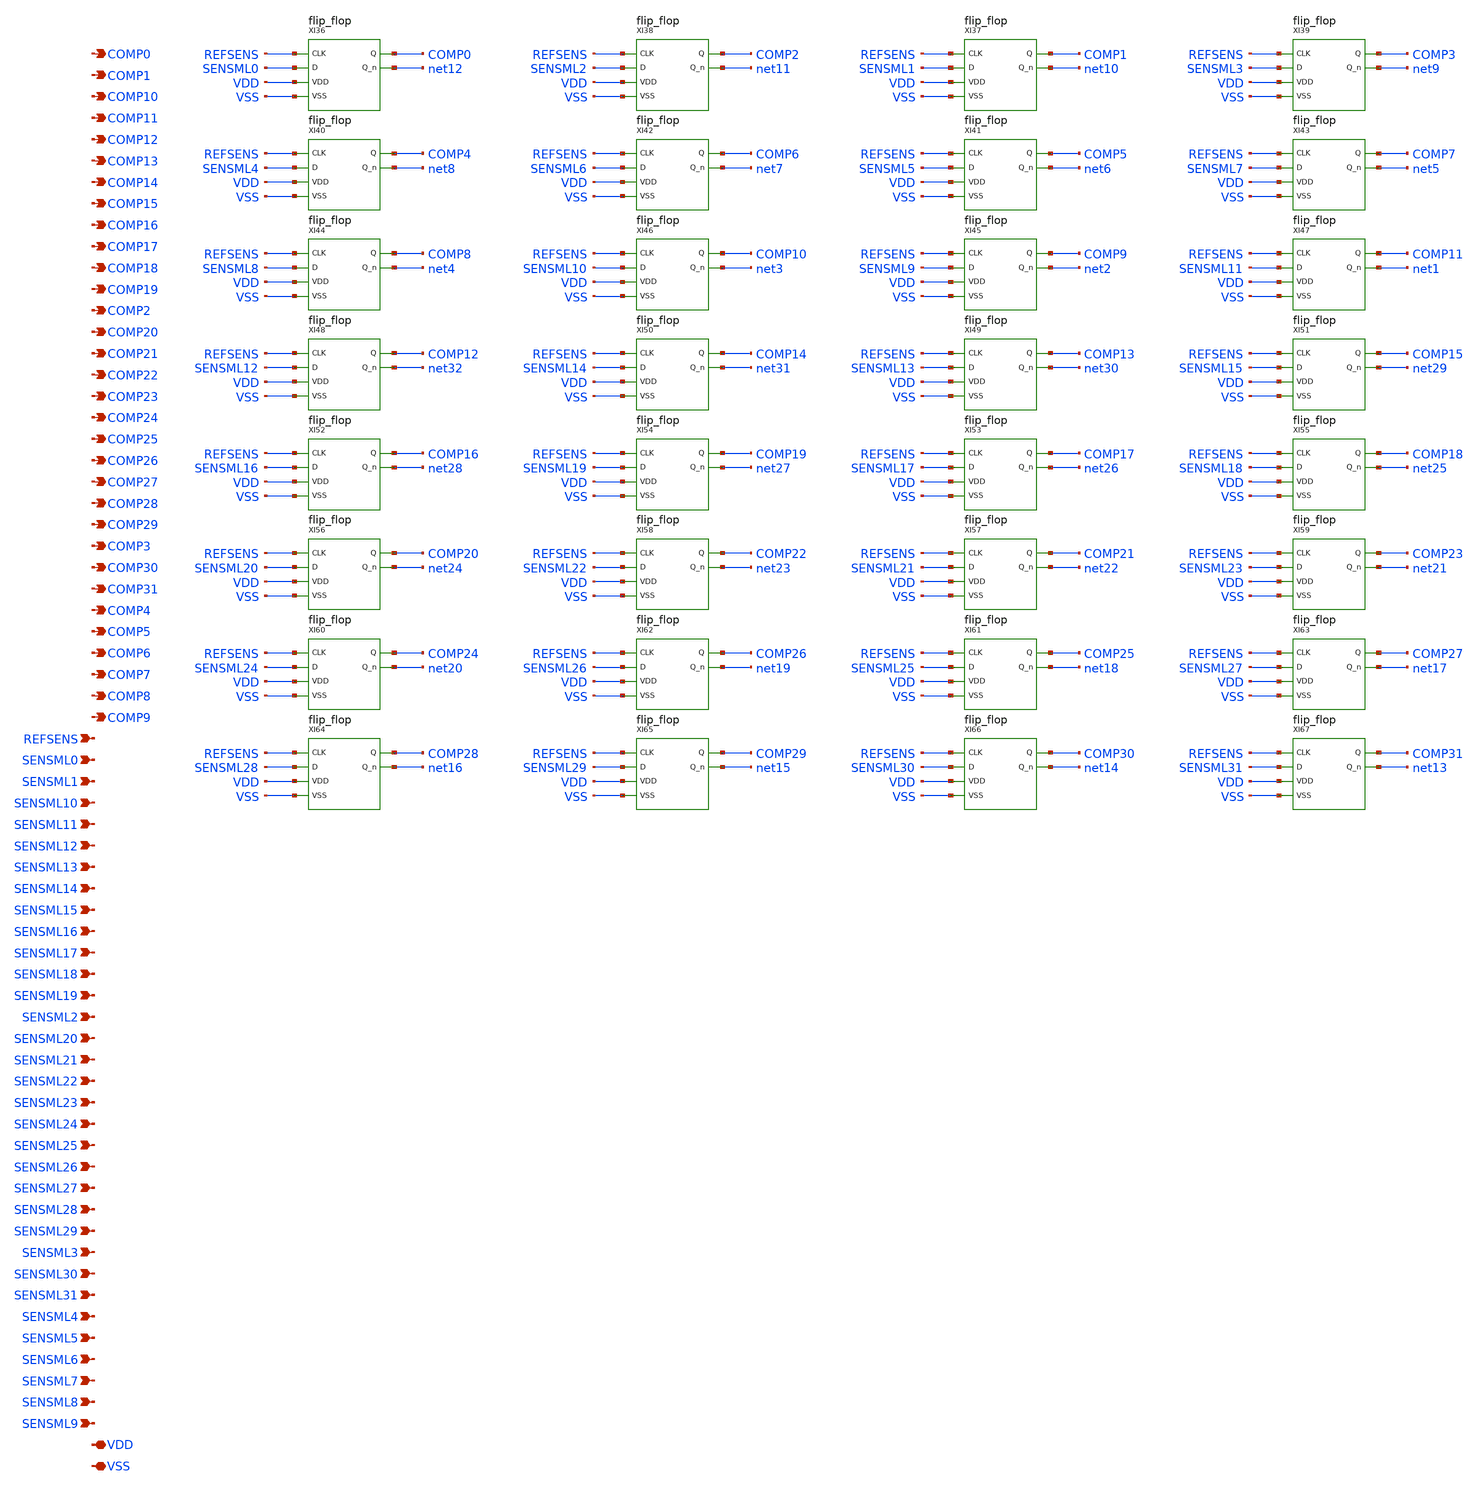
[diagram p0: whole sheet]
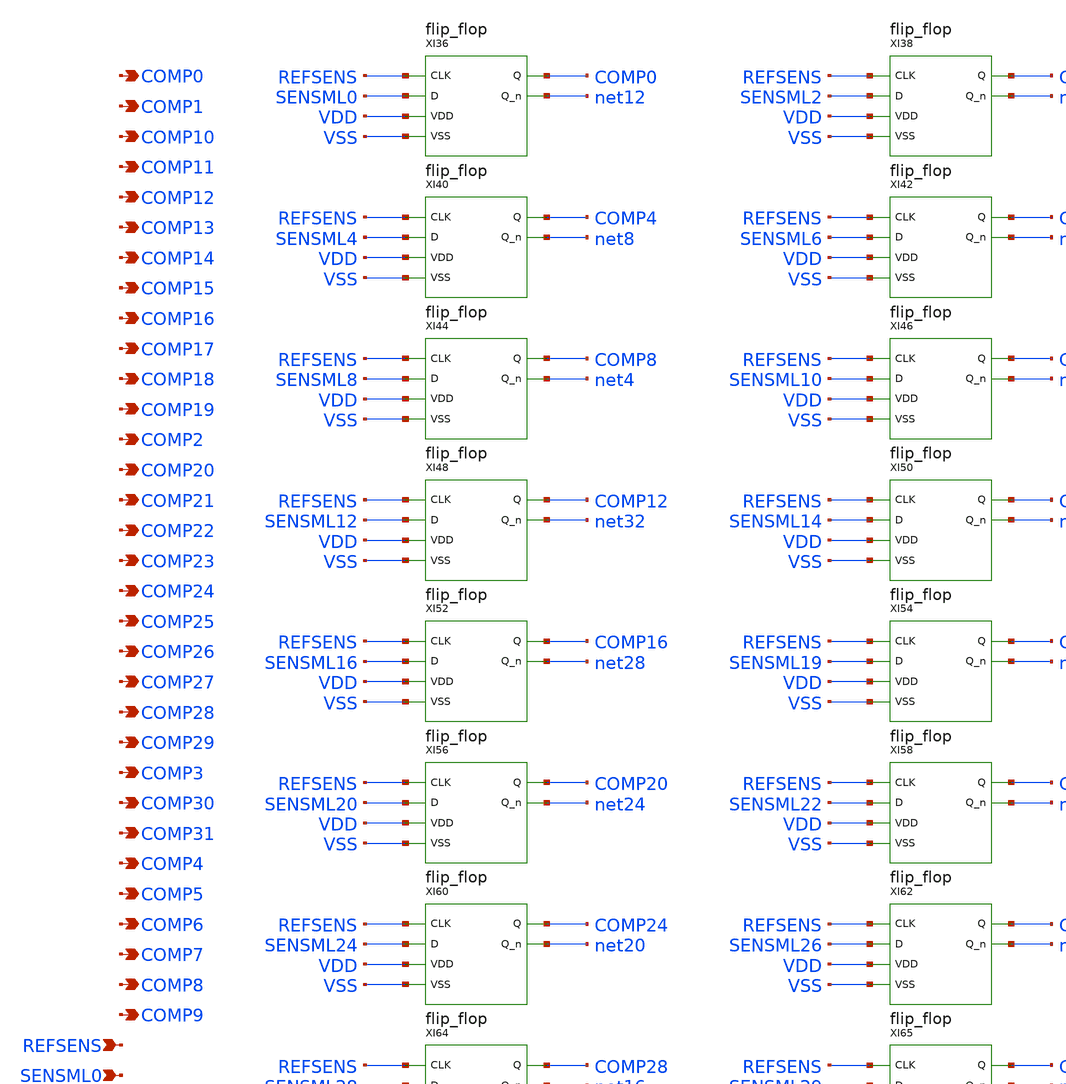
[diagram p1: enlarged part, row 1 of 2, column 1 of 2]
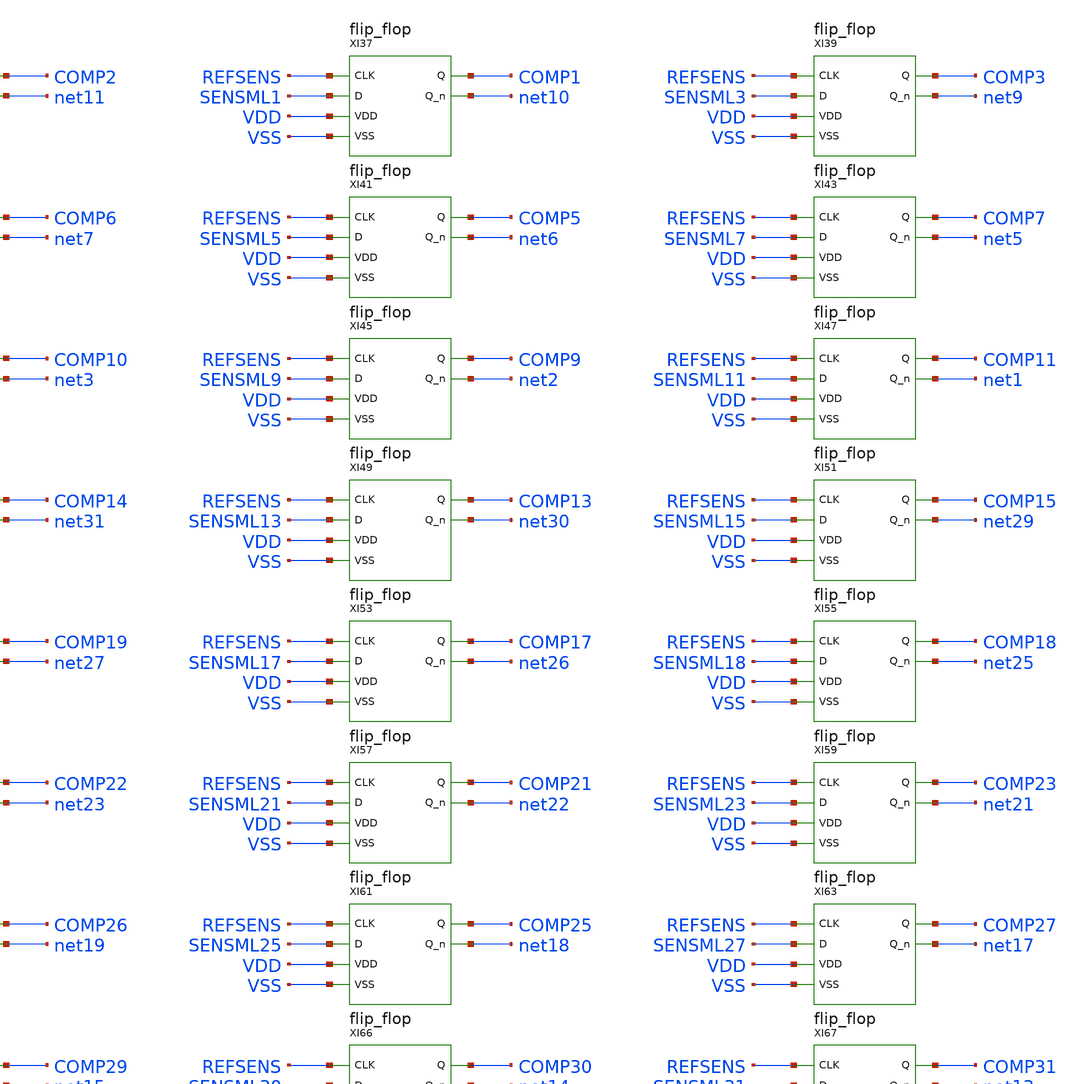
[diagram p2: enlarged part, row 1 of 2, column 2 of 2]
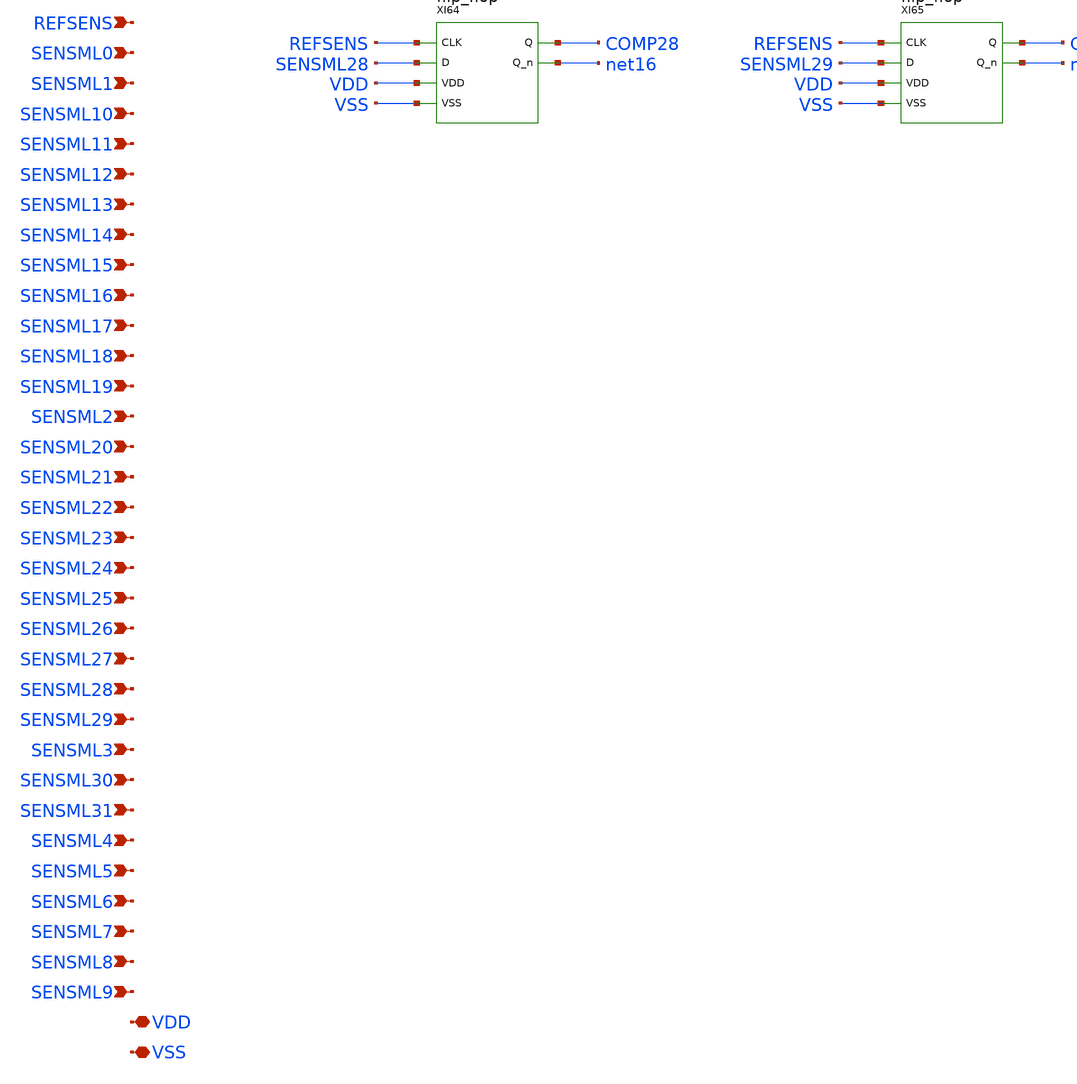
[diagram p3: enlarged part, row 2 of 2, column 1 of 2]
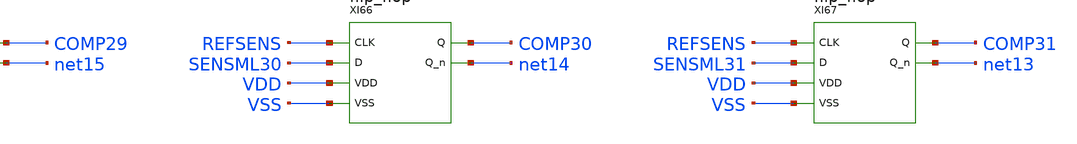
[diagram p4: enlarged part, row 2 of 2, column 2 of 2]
** sch_path: SoC6169-main/schematic/xschem/COMPARATOR_NEWBUFFER_64x32.sch
* Copyright 2026 USFQ CAM team
* Licensed under the Apache License, Version 2.0 (the "License");
* you may not use this file except in compliance with the License.
* You may obtain a copy of the License at
* https://www.apache.org/licenses/LICENSE-2.0
* Unless required by applicable law or agreed to in writing, software
* distributed under the License is distributed on an "AS IS" BASIS,
* WITHOUT WARRANTIES OR CONDITIONS OF ANY KIND, either express or implied.
* See the License for the specific language governing permissions and
* limitations under the License.
**.subckt COMPARATOR_NEWBUFFER_64x32 COMP0 COMP1 COMP10 COMP11 COMP12 COMP13 COMP14 COMP15 COMP16
*+ COMP17 COMP18 COMP19 COMP2 COMP20 COMP21 COMP22 COMP23 COMP24 COMP25 COMP26 COMP27 COMP28 COMP29 COMP3
*+ COMP30 COMP31 COMP4 COMP5 COMP6 COMP7 COMP8 COMP9 REFSENS SENSML0 SENSML1 SENSML10 SENSML11 SENSML12
*+ SENSML13 SENSML14 SENSML15 SENSML16 SENSML17 SENSML18 SENSML19 SENSML2 SENSML20 SENSML21 SENSML22 SENSML23
*+ SENSML24 SENSML25 SENSML26 SENSML27 SENSML28 SENSML29 SENSML3 SENSML30 SENSML31 SENSML4 SENSML5 SENSML6
*+ SENSML7 SENSML8 SENSML9 VDD VSS
*.opin COMP0
*.opin COMP1
*.opin COMP10
*.opin COMP11
*.opin COMP12
*.opin COMP13
*.opin COMP14
*.opin COMP15
*.opin COMP16
*.opin COMP17
*.opin COMP18
*.opin COMP19
*.opin COMP2
*.opin COMP20
*.opin COMP21
*.opin COMP22
*.opin COMP23
*.opin COMP24
*.opin COMP25
*.opin COMP26
*.opin COMP27
*.opin COMP28
*.opin COMP29
*.opin COMP3
*.opin COMP30
*.opin COMP31
*.opin COMP4
*.opin COMP5
*.opin COMP6
*.opin COMP7
*.opin COMP8
*.opin COMP9
*.ipin REFSENS
*.ipin SENSML0
*.ipin SENSML1
*.ipin SENSML10
*.ipin SENSML11
*.ipin SENSML12
*.ipin SENSML13
*.ipin SENSML14
*.ipin SENSML15
*.ipin SENSML16
*.ipin SENSML17
*.ipin SENSML18
*.ipin SENSML19
*.ipin SENSML2
*.ipin SENSML20
*.ipin SENSML21
*.ipin SENSML22
*.ipin SENSML23
*.ipin SENSML24
*.ipin SENSML25
*.ipin SENSML26
*.ipin SENSML27
*.ipin SENSML28
*.ipin SENSML29
*.ipin SENSML3
*.ipin SENSML30
*.ipin SENSML31
*.ipin SENSML4
*.ipin SENSML5
*.ipin SENSML6
*.ipin SENSML7
*.ipin SENSML8
*.ipin SENSML9
*.iopin VDD
*.iopin VSS
XI36 REFSENS SENSML0 COMP0 net12 VDD VSS flip_flop
XI38 REFSENS SENSML2 COMP2 net11 VDD VSS flip_flop
XI37 REFSENS SENSML1 COMP1 net10 VDD VSS flip_flop
XI39 REFSENS SENSML3 COMP3 net9 VDD VSS flip_flop
XI40 REFSENS SENSML4 COMP4 net8 VDD VSS flip_flop
XI42 REFSENS SENSML6 COMP6 net7 VDD VSS flip_flop
XI41 REFSENS SENSML5 COMP5 net6 VDD VSS flip_flop
XI43 REFSENS SENSML7 COMP7 net5 VDD VSS flip_flop
XI44 REFSENS SENSML8 COMP8 net4 VDD VSS flip_flop
XI46 REFSENS SENSML10 COMP10 net3 VDD VSS flip_flop
XI45 REFSENS SENSML9 COMP9 net2 VDD VSS flip_flop
XI47 REFSENS SENSML11 COMP11 net1 VDD VSS flip_flop
XI48 REFSENS SENSML12 COMP12 net32 VDD VSS flip_flop
XI50 REFSENS SENSML14 COMP14 net31 VDD VSS flip_flop
XI49 REFSENS SENSML13 COMP13 net30 VDD VSS flip_flop
XI51 REFSENS SENSML15 COMP15 net29 VDD VSS flip_flop
XI52 REFSENS SENSML16 COMP16 net28 VDD VSS flip_flop
XI54 REFSENS SENSML19 COMP19 net27 VDD VSS flip_flop
XI53 REFSENS SENSML17 COMP17 net26 VDD VSS flip_flop
XI55 REFSENS SENSML18 COMP18 net25 VDD VSS flip_flop
XI56 REFSENS SENSML20 COMP20 net24 VDD VSS flip_flop
XI58 REFSENS SENSML22 COMP22 net23 VDD VSS flip_flop
XI57 REFSENS SENSML21 COMP21 net22 VDD VSS flip_flop
XI59 REFSENS SENSML23 COMP23 net21 VDD VSS flip_flop
XI60 REFSENS SENSML24 COMP24 net20 VDD VSS flip_flop
XI62 REFSENS SENSML26 COMP26 net19 VDD VSS flip_flop
XI61 REFSENS SENSML25 COMP25 net18 VDD VSS flip_flop
XI63 REFSENS SENSML27 COMP27 net17 VDD VSS flip_flop
XI64 REFSENS SENSML28 COMP28 net16 VDD VSS flip_flop
XI65 REFSENS SENSML29 COMP29 net15 VDD VSS flip_flop
XI66 REFSENS SENSML30 COMP30 net14 VDD VSS flip_flop
XI67 REFSENS SENSML31 COMP31 net13 VDD VSS flip_flop
**.ends

* expanding   symbol:  flip_flop.sym # of pins=6
** sym_path: SoC6169-main/schematic/xschem/flip_flop.sym
** sch_path: SoC6169-main/schematic/xschem/flip_flop.sch
.subckt flip_flop CLK D Q Q_n VDD VSS
*.ipin CLK
*.ipin D
*.opin Q
*.opin Q_n
*.iopin VDD
*.iopin VSS
XI7 VSS Q_n VDD Q INV
XI5 VSS Q_n VDD net14 INV
XI4 VSS net17 VDD Q_n INV
XI3 VSS net9 VDD net15 INV
XI2 VSS CLK VDD net12 INV
XI1 VSS net8 VDD net9 INV
XI0 VSS D VDD net5 INV
XMN4 net17 net12 net14 VSS sg13_lv_nmos w=740n l=130n ng=1 m=1 mm_ok=1
XMN3 net9 CLK net17 VSS sg13_lv_nmos w=740n l=130n ng=1 m=1 mm_ok=1
XMN2 net8 CLK net15 VSS sg13_lv_nmos w=740n l=130n ng=1 m=1 mm_ok=1
XMN0 net5 net12 net8 VSS sg13_lv_nmos w=740n l=130n ng=1 m=1 mm_ok=1
XMP4 net17 CLK net14 VDD sg13_lv_pmos w=1120n l=130n ng=1 m=1 mm_ok=1
XMP3 net9 net12 net17 VDD sg13_lv_pmos w=1120n l=130n ng=1 m=1 mm_ok=1
XMP2 net8 net12 net15 VDD sg13_lv_pmos w=1120n l=130n ng=1 m=1 mm_ok=1
XMP0 net5 CLK net8 VDD sg13_lv_pmos w=1120n l=130n ng=1 m=1 mm_ok=1
.ends


* expanding   symbol:  INV.sym # of pins=4
** sym_path: SoC6169-main/schematic/xschem/INV.sym
** sch_path: SoC6169-main/schematic/xschem/INV.sch
.subckt INV GND IN VDD Y
*.iopin GND
*.ipin IN
*.iopin VDD
*.opin Y
XMN0 Y IN GND GND sg13_lv_nmos w=200n l=130n ng=1 m=1 mm_ok=1
XMP0 Y IN VDD VDD sg13_lv_pmos w=400n l=130n ng=1 m=1 mm_ok=1
.ends

.end
